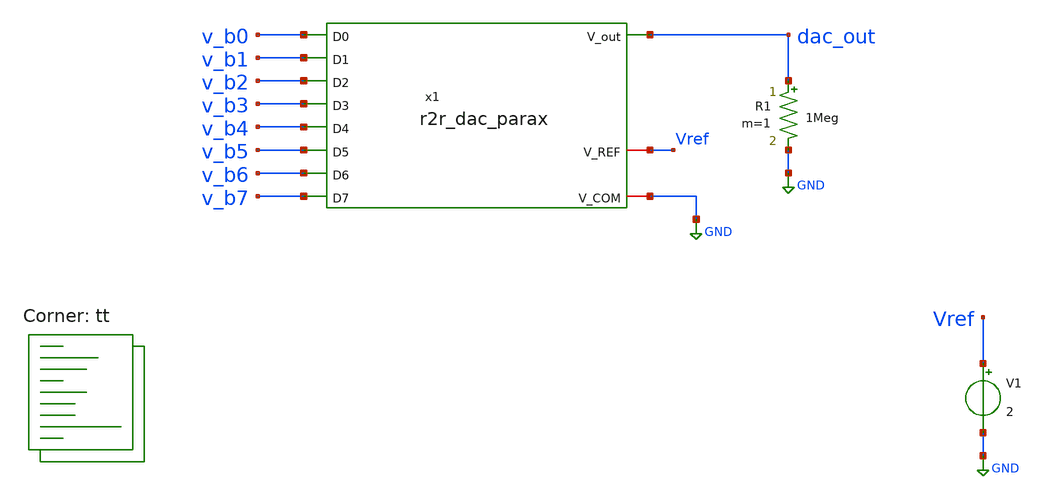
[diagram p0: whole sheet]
** sch_path: xschem/tb_dac_parax_perf.sch
**.subckt tb_dac_parax_perf
V1 Vref GND 2
x1 dac_out v_b7 v_b0 v_b1 v_b6 v_b2 v_b5 v_b3 v_b4 Vref GND r2r_dac_parax
R1 dac_out GND 1Meg m=1
**** begin user architecture code
.lib $::SKYWATER_MODELS/sky130.lib.spice tt


.include "stimuli_tb_dac_codes.cir"
.param v_hi = 1.8

.control

let index = 0
let loops = 8

repeat 1
save v(dac_out) v(v_b0) v(v_b1) v(v_b2) v(v_b3) v(v_b4) v(v_b5) v(v_b6) v(v_b7)
tran 100p 1290n
write tb_dac_parax_perf.raw
plot v(dac_out)
reset
end


*let x_ax = vector(loops)
*let v_high = vector(loops)
*let v_low = vector(loops)

*repeat $&loops
*end


.endc


**** end user architecture code
**.ends

* expanding   symbol:  r2r_dac_parax.sym # of pins=11
** sym_path: xschem/r2r_dac.sym
.include [file normalize extracted/r2r_dac_parax.spice]
.GLOBAL GND
.end
